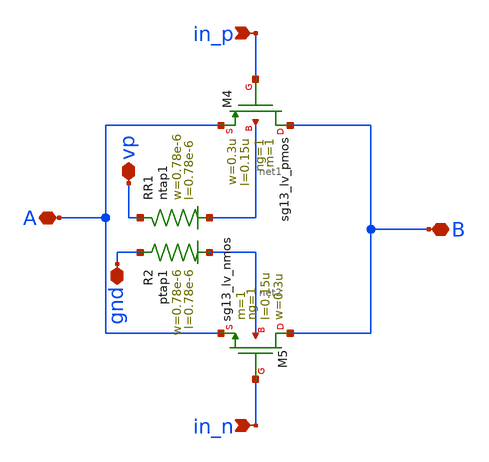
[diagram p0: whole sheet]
** sch_path: schematics/PFD/PFD_passgate.sch
**.subckt PFD_passgate in_n in_p vp gnd B A
*.ipin in_n
*.ipin in_p
*.iopin vp
*.iopin gnd
*.iopin B
*.iopin A
XM4 B in_p A net1 sg13_lv_pmos w=0.3u l=0.15u ng=1 m=1 mm_ok=1
XM5 B in_n A net2 sg13_lv_nmos w=0.3u l=0.15u ng=1 m=1 mm_ok=1
XR1 vp net1 ntap1 R=262.8 w=0.78e-6 l=0.78e-6
XR2 gnd net2 ptap1 R=262.8 w=0.78e-6 l=0.78e-6
**.ends
.end
